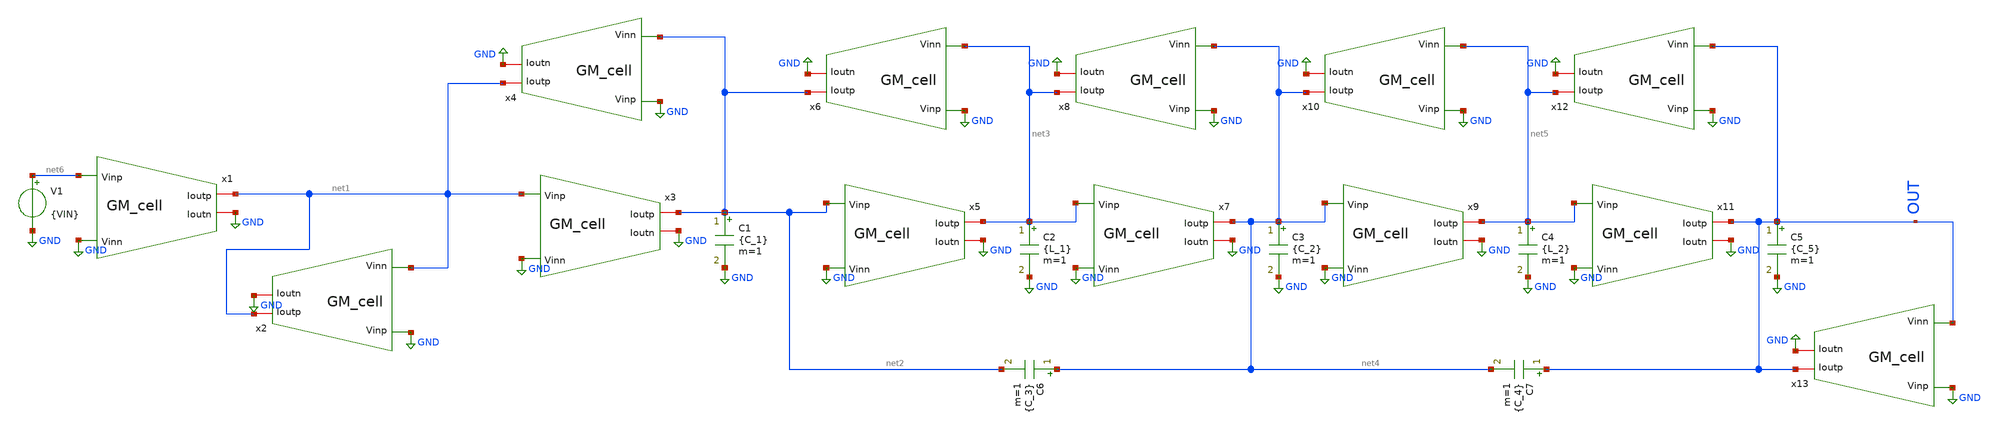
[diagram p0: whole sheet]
** sch_path: LPF design/SCLICAP_TEST/GM_C_filter2.sch
**.subckt GM_C_filter2
x1 net1 net6 GND GND GM_cell gm={k_1*gm_1} AV={AV_1}
x2 net1 GND net1 GND GM_cell gm={gm_1*k_s} AV={AV_1}
x3 net2 net1 GND GND GM_cell gm={k_1*gm_1} AV={AV_1}
x4 net1 GND net2 GND GM_cell gm={k_1*gm_1} AV={AV_1}
x5 net3 net2 GND GND GM_cell gm={k_1*gm_1} AV={AV_1}
x6 net2 GND net3 GND GM_cell gm={k_1*gm_1} AV={AV_1}
C1 net2 GND {C_1} m=1
C2 net3 GND {L_1} m=1
x7 net4 net3 GND GND GM_cell gm={k_1*gm_1} AV={AV_1}
x8 net3 GND net4 GND GM_cell gm={k_1*gm_1} AV={AV_1}
C3 net4 GND {C_2} m=1
x9 net5 net4 GND GND GM_cell gm={k_1*gm_1} AV={AV_1}
x10 net4 GND net5 GND GM_cell gm={k_1*gm_1} AV={AV_1}
C4 net5 GND {L_2} m=1
x11 OUT net5 GND GND GM_cell gm={k_1*gm_1} AV={AV_1}
x12 net5 GND OUT GND GM_cell gm={k_1*gm_1} AV={AV_1}
C5 OUT GND {C_5} m=1
x13 OUT GND OUT GND GM_cell gm={k_l*gm_1} AV={AV_1}
V1 net6 GND {VIN}
C6 net4 net2 {C_3} m=1
C7 OUT net4 {C_4} m=1
**.ends

* expanding   symbol:  GM_cell.sym # of pins=4
** sym_path: LPF design/SCLICAP_TEST/GM_cell.sym
** sch_path: LPF design/SCLICAP_TEST/GM_cell.sch
.subckt GM_cell Ioutp Vinp Vinn Ioutn  gm=100u AV=50
*.ipin Vinp
*.ipin Vinn
*.iopin Ioutn
*.iopin Ioutp
G1 Ioutn Ioutp Vinp Vinn {gm}
R1 Ioutn Ioutp {AV/gm} m=1
.ends

.GLOBAL GND
.end
